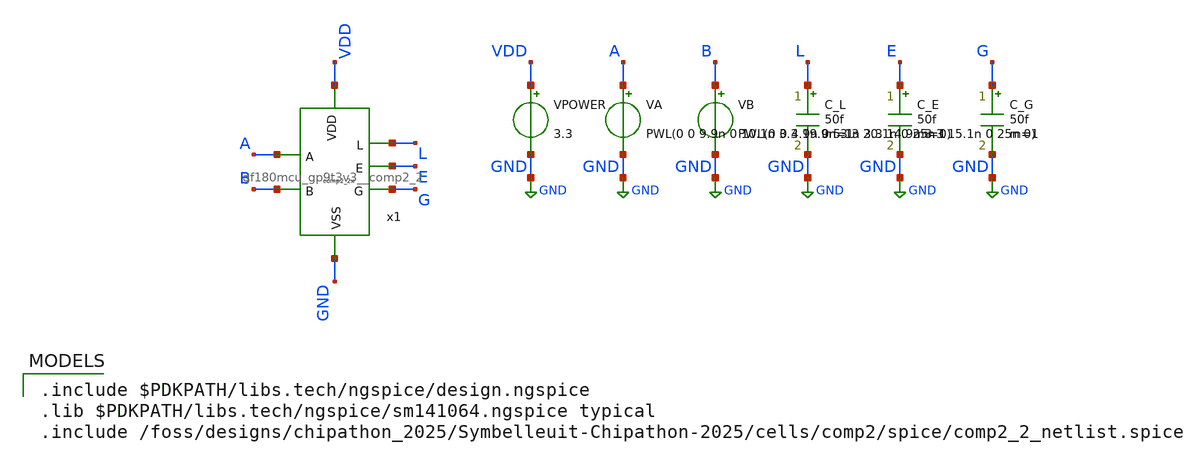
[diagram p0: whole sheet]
** sch_path: cells/comp2/cace/templates/comp2_2_tb_timing.sch
**.subckt comp2_2_tb_timing
x1 VDD L A E G B GND gf180mcu_gp9t3v3__comp2_2
VPOWER VDD GND 3.3
VA A GND PWL(0 0 9.9n 0 10.1n 3.3 19.9n 3.3 20.1n 0 25n 0)
VB B GND PWL(0 0 4.9n 0 5.1n 3.3 14.9n 3.3 15.1n 0 25n 0)
C_L L GND 50f m=1
C_E E GND 50f m=1
C_G G GND 50f m=1
**** begin user architecture code

.include $PDKPATH/libs.tech/ngspice/design.ngspice
.lib $PDKPATH/libs.tech/ngspice/sm141064.ngspice typical
.include /foss/designs/chipathon_2025/Symbelleuit-Chipathon-2025/cells/comp2/spice/comp2_2_netlist.spice


* CACE Timing Propagation Delay Simulation
.tran 50p 25n
.control
  run
  meas tran tpd_L_LH trig v(B) val=1.65 rise=1 targ v(L) val=1.65 rise=1
  meas tran tpd_E_HL trig v(B) val=1.65 rise=1 targ v(E) val=1.65 fall=1
  meas tran tpd_L_HL trig v(A) val=1.65 rise=1 targ v(L) val=1.65 fall=1
  meas tran tpd_E_LH trig v(A) val=1.65 rise=1 targ v(E) val=1.65 rise=1
  meas tran tpd_G_LH trig v(B) val=1.65 fall=1 targ v(G) val=1.65 rise=1
  meas tran tpd_G_HL trig v(A) val=1.65 fall=1 targ v(G) val=1.65 fall=1
  let tpd_max = max(max(tpd_L_LH, tpd_L_HL), max(max(tpd_G_LH, tpd_G_HL), max(tpd_E_LH, tpd_E_HL)))
  print tpd_max
  echo $&tpd_max > comp2_2_tb_timing_0.data
.endc
.GLOBAL GND


**** end user architecture code
**.ends

* expanding   symbol:  gf180mcu_gp9t3v3__comp2_2.sym # of pins=7
** sym_path: integration/cells/gf180mcu_gp9t3v3__comp2_2.sym
** sch_path: integration/cells/gf180mcu_gp9t3v3__comp2_2.sch
.subckt gf180mcu_gp9t3v3__comp2_2 VDD L A E G B VSS
*.opin L
*.opin G
*.opin E
*.ipin A
*.ipin B
*.ipin VDD
*.ipin VSS
XM17 net1 NOT_A VDD VDD pfet_03v3 L=0.3u W=1.7u nf=1 ad='int((nf+1)/2) * W/nf * 0.18u' as='int((nf+2)/2) * W/nf * 0.18u'
+ pd='2*int((nf+1)/2) * (W/nf + 0.18u)' ps='2*int((nf+2)/2) * (W/nf + 0.18u)' nrd='0.18u / W' nrs='0.18u / W'
+ sa=0 sb=0 sd=0 m=1
XM18 E NOT_B net1 VDD pfet_03v3 L=0.3u W=1.7u nf=1 ad='int((nf+1)/2) * W/nf * 0.18u' as='int((nf+2)/2) * W/nf * 0.18u'
+ pd='2*int((nf+1)/2) * (W/nf + 0.18u)' ps='2*int((nf+2)/2) * (W/nf + 0.18u)' nrd='0.18u / W' nrs='0.18u / W'
+ sa=0 sb=0 sd=0 m=1
XM19 net1 B VDD VDD pfet_03v3 L=0.3u W=3.4u nf=2 ad='int((nf+1)/2) * W/nf * 0.18u' as='int((nf+2)/2) * W/nf * 0.18u'
+ pd='2*int((nf+1)/2) * (W/nf + 0.18u)' ps='2*int((nf+2)/2) * (W/nf + 0.18u)' nrd='0.18u / W' nrs='0.18u / W'
+ sa=0 sb=0 sd=0 m=1
XM20 E A net1 VDD pfet_03v3 L=0.3u W=3.4u nf=2 ad='int((nf+1)/2) * W/nf * 0.18u' as='int((nf+2)/2) * W/nf * 0.18u'
+ pd='2*int((nf+1)/2) * (W/nf + 0.18u)' ps='2*int((nf+2)/2) * (W/nf + 0.18u)' nrd='0.18u / W' nrs='0.18u / W'
+ sa=0 sb=0 sd=0 m=1
XM21 E NOT_A net2 VSS nfet_03v3 L=0.3u W=0.85u nf=1 ad='int((nf+1)/2) * W/nf * 0.18u' as='int((nf+2)/2) * W/nf * 0.18u'
+ pd='2*int((nf+1)/2) * (W/nf + 0.18u)' ps='2*int((nf+2)/2) * (W/nf + 0.18u)' nrd='0.18u / W' nrs='0.18u / W'
+ sa=0 sb=0 sd=0 m=1
XM22 net2 B VSS VSS nfet_03v3 L=0.3u W=0.85u nf=1 ad='int((nf+1)/2) * W/nf * 0.18u' as='int((nf+2)/2) * W/nf * 0.18u'
+ pd='2*int((nf+1)/2) * (W/nf + 0.18u)' ps='2*int((nf+2)/2) * (W/nf + 0.18u)' nrd='0.18u / W' nrs='0.18u / W'
+ sa=0 sb=0 sd=0 m=1
XM23 E A net3 VSS nfet_03v3 L=0.3u W=1.7u nf=2 ad='int((nf+1)/2) * W/nf * 0.18u' as='int((nf+2)/2) * W/nf * 0.18u'
+ pd='2*int((nf+1)/2) * (W/nf + 0.18u)' ps='2*int((nf+2)/2) * (W/nf + 0.18u)' nrd='0.18u / W' nrs='0.18u / W'
+ sa=0 sb=0 sd=0 m=1
XM24 net3 NOT_B VSS VSS nfet_03v3 L=0.3u W=1.7u nf=2 ad='int((nf+1)/2) * W/nf * 0.18u' as='int((nf+2)/2) * W/nf * 0.18u'
+ pd='2*int((nf+1)/2) * (W/nf + 0.18u)' ps='2*int((nf+2)/2) * (W/nf + 0.18u)' nrd='0.18u / W' nrs='0.18u / W'
+ sa=0 sb=0 sd=0 m=1
XM1 NOT_B B VSS VSS nfet_03v3 L=0.3u W=0.85u nf=1 ad='int((nf+1)/2) * W/nf * 0.18u' as='int((nf+2)/2) * W/nf * 0.18u'
+ pd='2*int((nf+1)/2) * (W/nf + 0.18u)' ps='2*int((nf+2)/2) * (W/nf + 0.18u)' nrd='0.18u / W' nrs='0.18u / W'
+ sa=0 sb=0 sd=0 m=1
XM2 NOT_B B VDD VDD pfet_03v3 L=0.3u W=1.7u nf=1 ad='int((nf+1)/2) * W/nf * 0.18u' as='int((nf+2)/2) * W/nf * 0.18u'
+ pd='2*int((nf+1)/2) * (W/nf + 0.18u)' ps='2*int((nf+2)/2) * (W/nf + 0.18u)' nrd='0.18u / W' nrs='0.18u / W'
+ sa=0 sb=0 sd=0 m=1
XM3 NOT_A A VSS VSS nfet_03v3 L=0.3u W=0.85u nf=1 ad='int((nf+1)/2) * W/nf * 0.18u' as='int((nf+2)/2) * W/nf * 0.18u'
+ pd='2*int((nf+1)/2) * (W/nf + 0.18u)' ps='2*int((nf+2)/2) * (W/nf + 0.18u)' nrd='0.18u / W' nrs='0.18u / W'
+ sa=0 sb=0 sd=0 m=1
XM4 NOT_A A VDD VDD pfet_03v3 L=0.3u W=1.7u nf=1 ad='int((nf+1)/2) * W/nf * 0.18u' as='int((nf+2)/2) * W/nf * 0.18u'
+ pd='2*int((nf+1)/2) * (W/nf + 0.18u)' ps='2*int((nf+2)/2) * (W/nf + 0.18u)' nrd='0.18u / W' nrs='0.18u / W'
+ sa=0 sb=0 sd=0 m=1
XM5 net5 NOT_A net4 VSS nfet_03v3 L=0.3u W=0.85u nf=1 ad='int((nf+1)/2) * W/nf * 0.18u' as='int((nf+2)/2) * W/nf * 0.18u'
+ pd='2*int((nf+1)/2) * (W/nf + 0.18u)' ps='2*int((nf+2)/2) * (W/nf + 0.18u)' nrd='0.18u / W' nrs='0.18u / W'
+ sa=0 sb=0 sd=0 m=1
XM6 net4 B VSS VSS nfet_03v3 L=0.3u W=0.85u nf=1 ad='int((nf+1)/2) * W/nf * 0.18u' as='int((nf+2)/2) * W/nf * 0.18u'
+ pd='2*int((nf+1)/2) * (W/nf + 0.18u)' ps='2*int((nf+2)/2) * (W/nf + 0.18u)' nrd='0.18u / W' nrs='0.18u / W'
+ sa=0 sb=0 sd=0 m=1
XM7 net5 B VDD VDD pfet_03v3 L=0.3u W=1.7u nf=1 ad='int((nf+1)/2) * W/nf * 0.18u' as='int((nf+2)/2) * W/nf * 0.18u'
+ pd='2*int((nf+1)/2) * (W/nf + 0.18u)' ps='2*int((nf+2)/2) * (W/nf + 0.18u)' nrd='0.18u / W' nrs='0.18u / W'
+ sa=0 sb=0 sd=0 m=1
XM8 net5 NOT_A VDD VDD pfet_03v3 L=0.3u W=1.7u nf=1 ad='int((nf+1)/2) * W/nf * 0.18u' as='int((nf+2)/2) * W/nf * 0.18u'
+ pd='2*int((nf+1)/2) * (W/nf + 0.18u)' ps='2*int((nf+2)/2) * (W/nf + 0.18u)' nrd='0.18u / W' nrs='0.18u / W'
+ sa=0 sb=0 sd=0 m=1
XM9 L net5 VSS VSS nfet_03v3 L=0.3u W=1.7u nf=2 ad='int((nf+1)/2) * W/nf * 0.18u' as='int((nf+2)/2) * W/nf * 0.18u'
+ pd='2*int((nf+1)/2) * (W/nf + 0.18u)' ps='2*int((nf+2)/2) * (W/nf + 0.18u)' nrd='0.18u / W' nrs='0.18u / W'
+ sa=0 sb=0 sd=0 m=1
XM10 L net5 VDD VDD pfet_03v3 L=0.3u W=3.4u nf=2 ad='int((nf+1)/2) * W/nf * 0.18u' as='int((nf+2)/2) * W/nf * 0.18u'
+ pd='2*int((nf+1)/2) * (W/nf + 0.18u)' ps='2*int((nf+2)/2) * (W/nf + 0.18u)' nrd='0.18u / W' nrs='0.18u / W'
+ sa=0 sb=0 sd=0 m=1
XM11 net7 NOT_B net6 VSS nfet_03v3 L=0.3u W=0.85u nf=1 ad='int((nf+1)/2) * W/nf * 0.18u' as='int((nf+2)/2) * W/nf * 0.18u'
+ pd='2*int((nf+1)/2) * (W/nf + 0.18u)' ps='2*int((nf+2)/2) * (W/nf + 0.18u)' nrd='0.18u / W' nrs='0.18u / W'
+ sa=0 sb=0 sd=0 m=1
XM12 net6 A VSS VSS nfet_03v3 L=0.3u W=0.85u nf=1 ad='int((nf+1)/2) * W/nf * 0.18u' as='int((nf+2)/2) * W/nf * 0.18u'
+ pd='2*int((nf+1)/2) * (W/nf + 0.18u)' ps='2*int((nf+2)/2) * (W/nf + 0.18u)' nrd='0.18u / W' nrs='0.18u / W'
+ sa=0 sb=0 sd=0 m=1
XM13 net7 NOT_B VDD VDD pfet_03v3 L=0.3u W=1.7u nf=1 ad='int((nf+1)/2) * W/nf * 0.18u' as='int((nf+2)/2) * W/nf * 0.18u'
+ pd='2*int((nf+1)/2) * (W/nf + 0.18u)' ps='2*int((nf+2)/2) * (W/nf + 0.18u)' nrd='0.18u / W' nrs='0.18u / W'
+ sa=0 sb=0 sd=0 m=1
XM14 net7 A VDD VDD pfet_03v3 L=0.3u W=1.7u nf=1 ad='int((nf+1)/2) * W/nf * 0.18u' as='int((nf+2)/2) * W/nf * 0.18u'
+ pd='2*int((nf+1)/2) * (W/nf + 0.18u)' ps='2*int((nf+2)/2) * (W/nf + 0.18u)' nrd='0.18u / W' nrs='0.18u / W'
+ sa=0 sb=0 sd=0 m=1
XM15 G net7 VSS VSS nfet_03v3 L=0.3u W=1.7u nf=2 ad='int((nf+1)/2) * W/nf * 0.18u' as='int((nf+2)/2) * W/nf * 0.18u'
+ pd='2*int((nf+1)/2) * (W/nf + 0.18u)' ps='2*int((nf+2)/2) * (W/nf + 0.18u)' nrd='0.18u / W' nrs='0.18u / W'
+ sa=0 sb=0 sd=0 m=1
XM16 G net7 VDD VDD pfet_03v3 L=0.3u W=3.4u nf=2 ad='int((nf+1)/2) * W/nf * 0.18u' as='int((nf+2)/2) * W/nf * 0.18u'
+ pd='2*int((nf+1)/2) * (W/nf + 0.18u)' ps='2*int((nf+2)/2) * (W/nf + 0.18u)' nrd='0.18u / W' nrs='0.18u / W'
+ sa=0 sb=0 sd=0 m=1
.ends

.GLOBAL GND
.end
